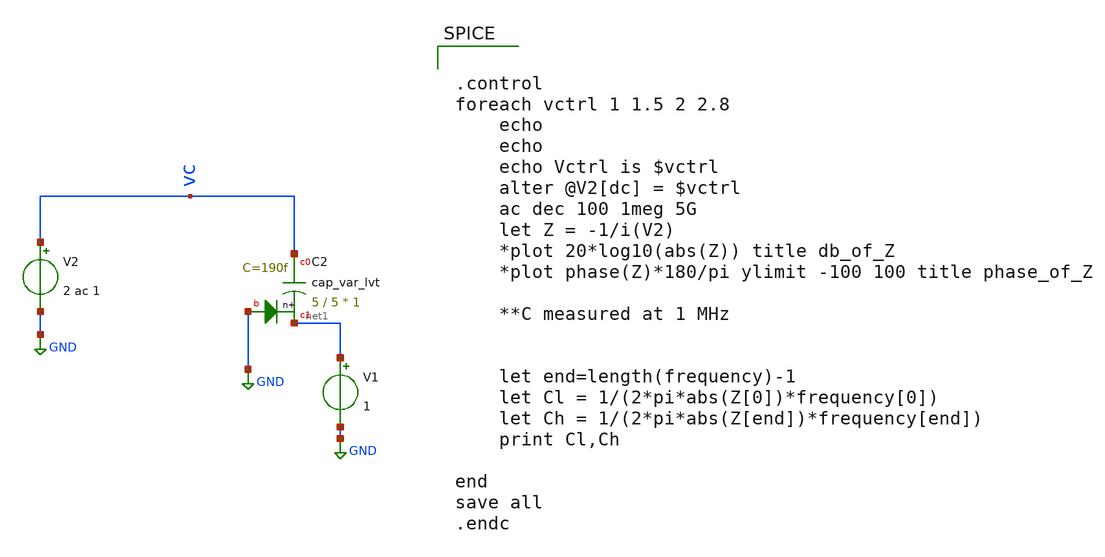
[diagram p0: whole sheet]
** sch_path: varactor_meas/varactor_ac.sch
**.subckt varactor_ac
V2 vc GND 2 ac 1
XC2 vc net1 GND sky130_fd_pr__cap_var_lvt W=5 L=5 VM=1 m=1
V1 net1 GND 1
**** begin user architecture code


.control
foreach vctrl 1 1.5 2 2.8
	echo
	echo
	echo Vctrl is $vctrl
	alter @V2[dc] = $vctrl
	ac dec 100 1meg 5G
	let Z = -1/i(V2)
	*plot 20*log10(abs(Z)) title db_of_Z
	*plot phase(Z)*180/pi ylimit -100 100 title phase_of_Z

	**C measured at 1 MHz


	let end=length(frequency)-1
	let Cl = 1/(2*pi*abs(Z[0])*frequency[0])
	let Ch = 1/(2*pi*abs(Z[end])*frequency[end])
	print Cl,Ch

end
save all
.endc




.option wnflag = 1
.lib /usr/local/share/pdk/sky130A/libs.tech/ngspice/sky130.lib.spice tt
.include /usr/local/share/pdk/sky130A/libs.ref/sky130_fd_pr/spice/sky130_fd_pr__ind_05_220.model.spice
.param mc_mm_switch=0


**** end user architecture code
**.ends
.GLOBAL GND
.end
